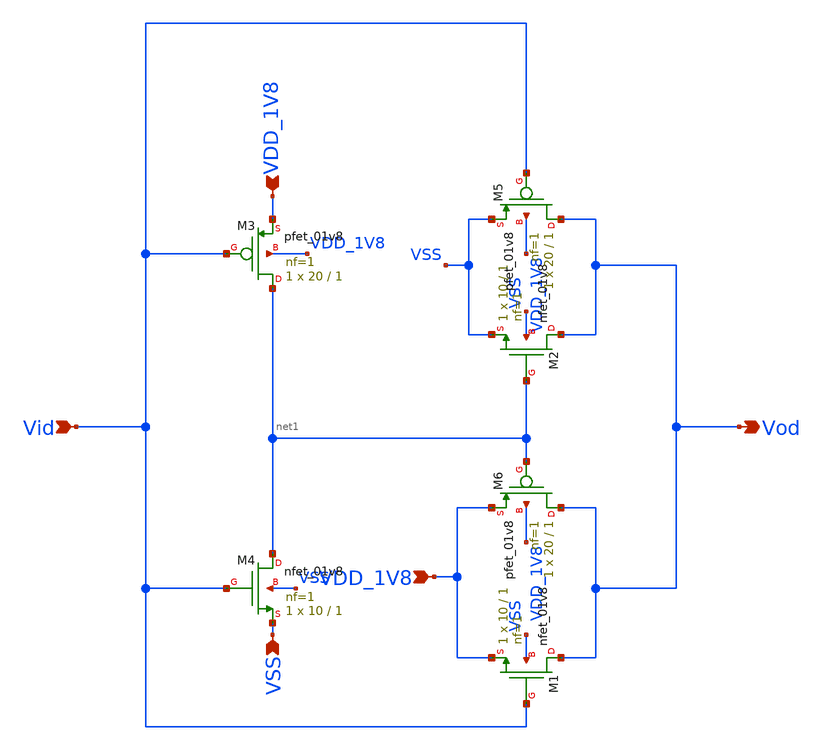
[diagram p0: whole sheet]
** sch_path: design/CNR_GR06_SKY130NM/dac_n.sch
**.subckt dac_n VDD_1V8 VSS Vid Vod VDD_1V8
*.ipin VDD_1V8
*.ipin VSS
*.ipin Vid
*.opin Vod
*.ipin VDD_1V8
XM3 net1 Vid VDD_1V8 VDD_1V8 sky130_fd_pr__pfet_01v8 L=1 W=20 nf=1 ad='int((nf+1)/2) * W/nf * 0.29' as='int((nf+2)/2) * W/nf * 0.29'
+ pd='2*int((nf+1)/2) * (W/nf + 0.29)' ps='2*int((nf+2)/2) * (W/nf + 0.29)' nrd='0.29 / W' nrs='0.29 / W'
+ sa=0 sb=0 sd=0 mult=1 m=1
XM4 net1 Vid VSS VSS sky130_fd_pr__nfet_01v8 L=1 W=10 nf=1 ad='int((nf+1)/2) * W/nf * 0.29' as='int((nf+2)/2) * W/nf * 0.29'
+ pd='2*int((nf+1)/2) * (W/nf + 0.29)' ps='2*int((nf+2)/2) * (W/nf + 0.29)' nrd='0.29 / W' nrs='0.29 / W'
+ sa=0 sb=0 sd=0 mult=1 m=1
XM1 Vod Vid VDD_1V8 VSS sky130_fd_pr__nfet_01v8 L=1 W=10 nf=1 ad='int((nf+1)/2) * W/nf * 0.29' as='int((nf+2)/2) * W/nf * 0.29'
+ pd='2*int((nf+1)/2) * (W/nf + 0.29)' ps='2*int((nf+2)/2) * (W/nf + 0.29)' nrd='0.29 / W' nrs='0.29 / W'
+ sa=0 sb=0 sd=0 mult=1 m=1
XM2 Vod net1 VSS VSS sky130_fd_pr__nfet_01v8 L=1 W=10 nf=1 ad='int((nf+1)/2) * W/nf * 0.29' as='int((nf+2)/2) * W/nf * 0.29'
+ pd='2*int((nf+1)/2) * (W/nf + 0.29)' ps='2*int((nf+2)/2) * (W/nf + 0.29)' nrd='0.29 / W' nrs='0.29 / W'
+ sa=0 sb=0 sd=0 mult=1 m=1
XM5 Vod Vid VSS VDD_1V8 sky130_fd_pr__pfet_01v8 L=1 W=20 nf=1 ad='int((nf+1)/2) * W/nf * 0.29' as='int((nf+2)/2) * W/nf * 0.29'
+ pd='2*int((nf+1)/2) * (W/nf + 0.29)' ps='2*int((nf+2)/2) * (W/nf + 0.29)' nrd='0.29 / W' nrs='0.29 / W'
+ sa=0 sb=0 sd=0 mult=1 m=1
XM6 Vod net1 VDD_1V8 VDD_1V8 sky130_fd_pr__pfet_01v8 L=1 W=20 nf=1 ad='int((nf+1)/2) * W/nf * 0.29' as='int((nf+2)/2) * W/nf * 0.29'
+ pd='2*int((nf+1)/2) * (W/nf + 0.29)' ps='2*int((nf+2)/2) * (W/nf + 0.29)' nrd='0.29 / W' nrs='0.29 / W'
+ sa=0 sb=0 sd=0 mult=1 m=1
**.ends
.end
